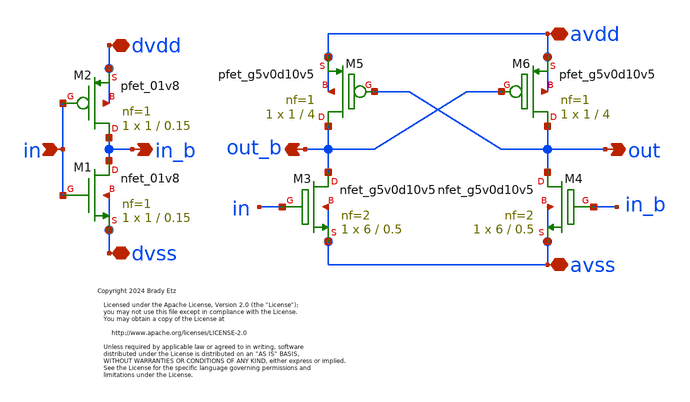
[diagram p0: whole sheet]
** sch_path: xschem/level_shift_tiny.sch
* Copyright 2024 Brady Etz
* Licensed under the Apache License, Version 2.0 (the "License");
**.subckt level_shift_tiny in avdd avss dvss dvdd out out_b in_b
*.ipin in
*.iopin avdd
*.iopin avss
*.iopin dvss
*.iopin dvdd
*.opin out
*.opin out_b
*.opin in_b
XM4 out in_b avss avss sky130_fd_pr__nfet_g5v0d10v5 L=0.5 W=6 nf=2 ad='int((nf+1)/2) * W/nf * 0.29' as='int((nf+2)/2) * W/nf * 0.29'
+ pd='2*int((nf+1)/2) * (W/nf + 0.29)' ps='2*int((nf+2)/2) * (W/nf + 0.29)' nrd='0.29 / W' nrs='0.29 / W'
+ sa=0 sb=0 sd=0 mult=1 m=1
XM3 out_b in avss avss sky130_fd_pr__nfet_g5v0d10v5 L=0.5 W=6 nf=2 ad='int((nf+1)/2) * W/nf * 0.29' as='int((nf+2)/2) * W/nf * 0.29'
+ pd='2*int((nf+1)/2) * (W/nf + 0.29)' ps='2*int((nf+2)/2) * (W/nf + 0.29)' nrd='0.29 / W' nrs='0.29 / W'
+ sa=0 sb=0 sd=0 mult=1 m=1
XM5 out_b out avdd avdd sky130_fd_pr__pfet_g5v0d10v5 L=4 W=1 nf=1 ad='int((nf+1)/2) * W/nf * 0.29' as='int((nf+2)/2) * W/nf * 0.29'
+ pd='2*int((nf+1)/2) * (W/nf + 0.29)' ps='2*int((nf+2)/2) * (W/nf + 0.29)' nrd='0.29 / W' nrs='0.29 / W'
+ sa=0 sb=0 sd=0 mult=1 m=1
XM6 out out_b avdd avdd sky130_fd_pr__pfet_g5v0d10v5 L=4 W=1 nf=1 ad='int((nf+1)/2) * W/nf * 0.29' as='int((nf+2)/2) * W/nf * 0.29'
+ pd='2*int((nf+1)/2) * (W/nf + 0.29)' ps='2*int((nf+2)/2) * (W/nf + 0.29)' nrd='0.29 / W' nrs='0.29 / W'
+ sa=0 sb=0 sd=0 mult=1 m=1
XM2 in_b in dvdd dvdd sky130_fd_pr__pfet_01v8 L=0.15 W=1 nf=1 ad='int((nf+1)/2) * W/nf * 0.29' as='int((nf+2)/2) * W/nf * 0.29'
+ pd='2*int((nf+1)/2) * (W/nf + 0.29)' ps='2*int((nf+2)/2) * (W/nf + 0.29)' nrd='0.29 / W' nrs='0.29 / W'
+ sa=0 sb=0 sd=0 mult=1 m=1
XM1 in_b in dvss dvss sky130_fd_pr__nfet_01v8 L=0.15 W=1 nf=1 ad='int((nf+1)/2) * W/nf * 0.29' as='int((nf+2)/2) * W/nf * 0.29'
+ pd='2*int((nf+1)/2) * (W/nf + 0.29)' ps='2*int((nf+2)/2) * (W/nf + 0.29)' nrd='0.29 / W' nrs='0.29 / W'
+ sa=0 sb=0 sd=0 mult=1 m=1
**.ends
.end
